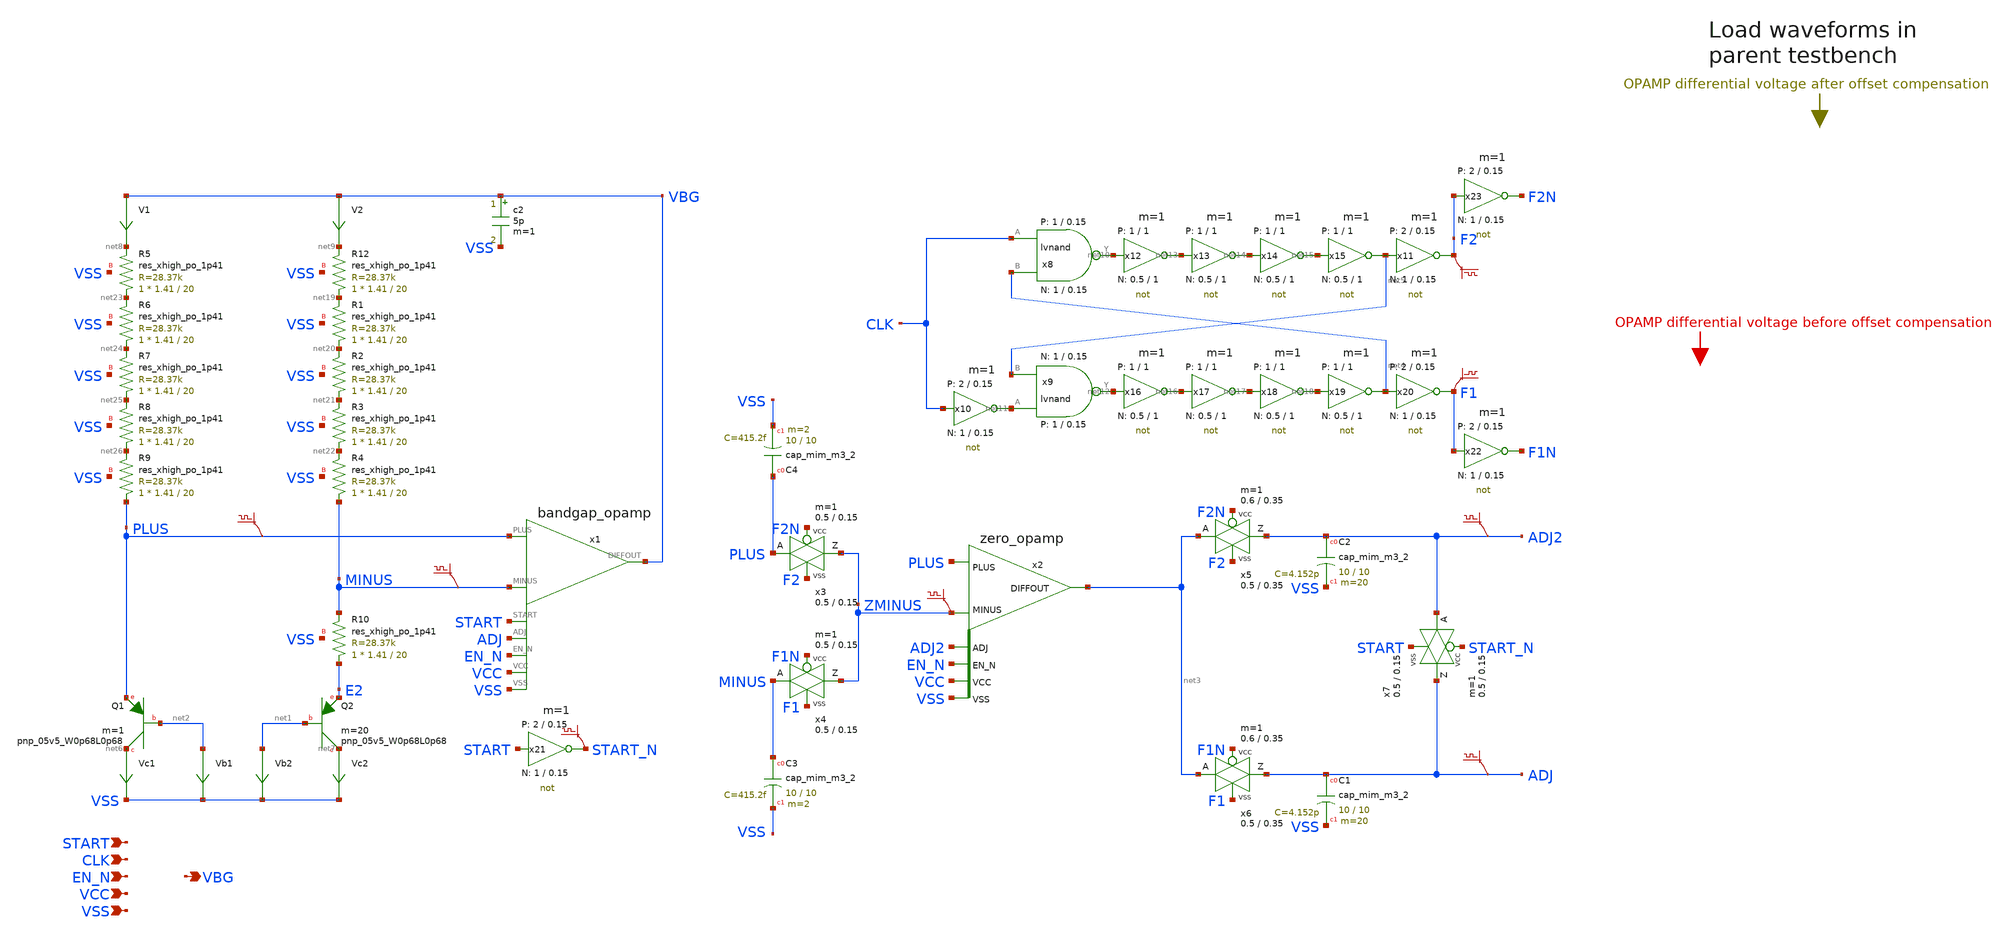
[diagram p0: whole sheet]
** sch_path: sky130A/xschem_libs/sky130_tests_ase/bandgap/schematic/bandgap.sch
* Copyright 2021 Stefan Frederik Schippers
* Licensed under the Apache License, Version 2.0 (the "License");
* you may not use this file except in compliance with the License.
* You may obtain a copy of the License at
* https://www.apache.org/licenses/LICENSE-2.0
* Unless required by applicable law or agreed to in writing, software
* distributed under the License is distributed on an "AS IS" BASIS,
* WITHOUT WARRANTIES OR CONDITIONS OF ANY KIND, either express or implied.
* See the License for the specific language governing permissions and
* limitations under the License.
**.subckt bandgap EN_N VBG VCC VSS CLK START
*.ipin EN_N
*.opin VBG
*.ipin VCC
*.ipin VSS
*.ipin CLK
*.ipin START
XQ1 net6 net2 PLUS sky130_fd_pr__pnp_05v5_W0p68L0p68 m=1
XQ2 net7 net1 E2 sky130_fd_pr__pnp_05v5_W0p68L0p68 m=20
Vc1 net6 VSS 0
.save i(vc1)
Vb1 net2 VSS 0
.save i(vb1)
Vb2 net1 VSS 0
.save i(vb2)
Vc2 net7 VSS 0
.save i(vc2)
x1 EN_N MINUS PLUS VBG VCC VSS ADJ START bandgap_opamp
V1 VBG net8 0
.save i(v1)
V2 VBG net9 0
.save i(v2)
x2 EN_N ZMINUS PLUS net3 VCC VSS ADJ2 zero_opamp
x3 ZMINUS PLUS F2N F2 VCC VSS passgate W_N=0.5 L_N=0.15 W_P=0.5 L_P=0.15 m=1
x4 ZMINUS MINUS F1N F1 VCC VSS passgate W_N=0.5 L_N=0.15 W_P=0.5 L_P=0.15 m=1
x5 ADJ2 net3 F2N F2 VCC VSS passgate_lvtp W_N=0.5 L_N=0.35 W_P=0.6 L_P=0.35 m=1
x6 ADJ net3 F1N F1 VCC VSS passgate_lvtp W_N=0.5 L_N=0.35 W_P=0.6 L_P=0.35 m=1
x8 CLK net4 net10 VCC VSS lvnand WidthN=1 LenN=0.15 WidthP=1 LenP=0.15 m=1
x9 net11 net5 net12 VCC VSS lvnand WidthN=1 LenN=0.15 WidthP=1 LenP=0.15 m=1
x10 net11 CLK VCC VSS not W_N=1 L_N=0.15 W_P=2 L_P=0.15 m=1
x11 F2 net5 VCC VSS not W_N=1 L_N=0.15 W_P=2 L_P=0.15 m=1
x12 net13 net10 VCC VSS not W_N=0.5 L_N=1 W_P=1 L_P=1 m=1
x13 net14 net13 VCC VSS not W_N=0.5 L_N=1 W_P=1 L_P=1 m=1
x14 net15 net14 VCC VSS not W_N=0.5 L_N=1 W_P=1 L_P=1 m=1
x15 net5 net15 VCC VSS not W_N=0.5 L_N=1 W_P=1 L_P=1 m=1
x16 net16 net12 VCC VSS not W_N=0.5 L_N=1 W_P=1 L_P=1 m=1
x17 net17 net16 VCC VSS not W_N=0.5 L_N=1 W_P=1 L_P=1 m=1
x18 net18 net17 VCC VSS not W_N=0.5 L_N=1 W_P=1 L_P=1 m=1
x19 net4 net18 VCC VSS not W_N=0.5 L_N=1 W_P=1 L_P=1 m=1
x20 F1 net4 VCC VSS not W_N=1 L_N=0.15 W_P=2 L_P=0.15 m=1
c2 VBG VSS 5p m=1
x7 ADJ ADJ2 START_N START VCC VSS passgate W_N=0.5 L_N=0.15 W_P=0.5 L_P=0.15 m=1
x21 START_N START VCC VSS not W_N=1 L_N=0.15 W_P=2 L_P=0.15 m=1
x22 F1N F1 VCC VSS not W_N=1 L_N=0.15 W_P=2 L_P=0.15 m=1
x23 F2N F2 VCC VSS not W_N=1 L_N=0.15 W_P=2 L_P=0.15 m=1
XC2 ADJ2 VSS sky130_fd_pr__cap_mim_m3_2 W=10 L=10 MF=20 m=20
XC1 ADJ VSS sky130_fd_pr__cap_mim_m3_2 W=10 L=10 MF=20 m=20
.save v(adj2)
.save v(adj)
.save v(f1)
.save v(f2)
.save v(zminus)
.save v(plus)
.save v(minus)
.save v(start_n)
XR12 net19 net9 VSS sky130_fd_pr__res_xhigh_po_1p41 L=20 mult=1 m=1
XR1 net20 net19 VSS sky130_fd_pr__res_xhigh_po_1p41 L=20 mult=1 m=1
XR2 net21 net20 VSS sky130_fd_pr__res_xhigh_po_1p41 L=20 mult=1 m=1
XR3 net22 net21 VSS sky130_fd_pr__res_xhigh_po_1p41 L=20 mult=1 m=1
XR4 MINUS net22 VSS sky130_fd_pr__res_xhigh_po_1p41 L=20 mult=1 m=1
XR5 net23 net8 VSS sky130_fd_pr__res_xhigh_po_1p41 L=20 mult=1 m=1
XR6 net24 net23 VSS sky130_fd_pr__res_xhigh_po_1p41 L=20 mult=1 m=1
XR7 net25 net24 VSS sky130_fd_pr__res_xhigh_po_1p41 L=20 mult=1 m=1
XR8 net26 net25 VSS sky130_fd_pr__res_xhigh_po_1p41 L=20 mult=1 m=1
XR9 PLUS net26 VSS sky130_fd_pr__res_xhigh_po_1p41 L=20 mult=1 m=1
XR10 E2 MINUS VSS sky130_fd_pr__res_xhigh_po_1p41 L=20 mult=1 m=1
XC3 MINUS VSS sky130_fd_pr__cap_mim_m3_2 W=10 L=10 MF=2 m=2
XC4 PLUS VSS sky130_fd_pr__cap_mim_m3_2 W=10 L=10 MF=2 m=2
**.ends
.end
